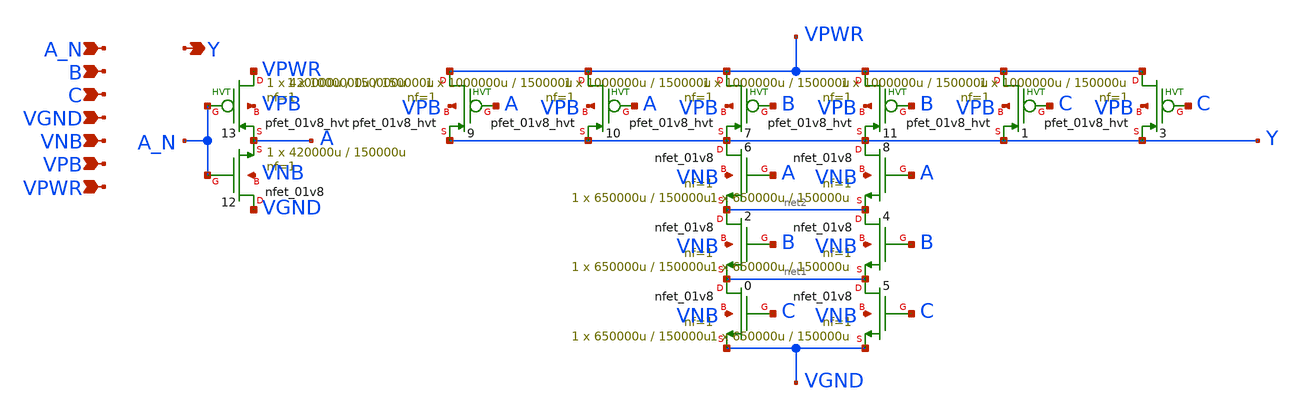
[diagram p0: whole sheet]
** sch_path: schematics/nand3b/sky130_fd_sc_hd__nand3b_2.sch
**.subckt sky130_fd_sc_hd__nand3b_2 A_N B C VGND VNB VPB VPWR Y
*.ipin A_N
*.ipin B
*.ipin C
*.ipin VGND
*.ipin VNB
*.ipin VPB
*.ipin VPWR
*.opin Y
X10 VPWR A Y VPB sky130_fd_pr__pfet_01v8_hvt L=150000u W=1000000u nf=1 ad='int((1 + 1)/2) * 1000000u / 1 * 0.29'
+ as='int((1 + 2)/2) * 1000000u / 1 * 0.29' pd='2*int((1 + 1)/2) * (1000000u / 1 + 0.29)' ps='2*int((1 + 2)/2) * (1000000u / 1 + 0.29)'
+ nrd='0.29 / 1000000u ' nrs='0.29 / 1000000u ' sa=0 sb=0 sd=0 mult=1 m=1
X9 VPWR A Y VPB sky130_fd_pr__pfet_01v8_hvt L=150000u W=1000000u nf=1 ad='int((1 + 1)/2) * 1000000u / 1 * 0.29'
+ as='int((1 + 2)/2) * 1000000u / 1 * 0.29' pd='2*int((1 + 1)/2) * (1000000u / 1 + 0.29)' ps='2*int((1 + 2)/2) * (1000000u / 1 + 0.29)'
+ nrd='0.29 / 1000000u ' nrs='0.29 / 1000000u ' sa=0 sb=0 sd=0 mult=1 m=1
X6 Y A net2 VNB sky130_fd_pr__nfet_01v8 L=150000u W=650000u nf=1 ad='int((1 + 1)/2) * 650000u / 1 * 0.29'
+ as='int((1 + 2)/2) * 650000u / 1 * 0.29' pd='2*int((1 + 1)/2) * (650000u / 1 + 0.29)' ps='2*int((1 + 2)/2) * (650000u / 1 + 0.29)'
+ nrd='0.29 / 650000u ' nrs='0.29 / 650000u ' sa=0 sb=0 sd=0 mult=1 m=1
X2 net2 B net1 VNB sky130_fd_pr__nfet_01v8 L=150000u W=650000u nf=1 ad='int((1 + 1)/2) * 650000u / 1 * 0.29'
+ as='int((1 + 2)/2) * 650000u / 1 * 0.29' pd='2*int((1 + 1)/2) * (650000u / 1 + 0.29)' ps='2*int((1 + 2)/2) * (650000u / 1 + 0.29)'
+ nrd='0.29 / 650000u ' nrs='0.29 / 650000u ' sa=0 sb=0 sd=0 mult=1 m=1
X7 VPWR B Y VPB sky130_fd_pr__pfet_01v8_hvt L=150000u W=1000000u nf=1 ad='int((1 + 1)/2) * 1000000u / 1 * 0.29'
+ as='int((1 + 2)/2) * 1000000u / 1 * 0.29' pd='2*int((1 + 1)/2) * (1000000u / 1 + 0.29)' ps='2*int((1 + 2)/2) * (1000000u / 1 + 0.29)'
+ nrd='0.29 / 1000000u ' nrs='0.29 / 1000000u ' sa=0 sb=0 sd=0 mult=1 m=1
X0 net1 C VGND VNB sky130_fd_pr__nfet_01v8 L=150000u W=650000u nf=1 ad='int((1 + 1)/2) * 650000u / 1 * 0.29'
+ as='int((1 + 2)/2) * 650000u / 1 * 0.29' pd='2*int((1 + 1)/2) * (650000u / 1 + 0.29)' ps='2*int((1 + 2)/2) * (650000u / 1 + 0.29)'
+ nrd='0.29 / 650000u ' nrs='0.29 / 650000u ' sa=0 sb=0 sd=0 mult=1 m=1
X1 VPWR C Y VPB sky130_fd_pr__pfet_01v8_hvt L=150000u W=1000000u nf=1 ad='int((1 + 1)/2) * 1000000u / 1 * 0.29'
+ as='int((1 + 2)/2) * 1000000u / 1 * 0.29' pd='2*int((1 + 1)/2) * (1000000u / 1 + 0.29)' ps='2*int((1 + 2)/2) * (1000000u / 1 + 0.29)'
+ nrd='0.29 / 1000000u ' nrs='0.29 / 1000000u ' sa=0 sb=0 sd=0 mult=1 m=1
X11 VPWR B Y VPB sky130_fd_pr__pfet_01v8_hvt L=150000u W=1000000u nf=1 ad='int((1 + 1)/2) * 1000000u / 1 * 0.29'
+ as='int((1 + 2)/2) * 1000000u / 1 * 0.29' pd='2*int((1 + 1)/2) * (1000000u / 1 + 0.29)' ps='2*int((1 + 2)/2) * (1000000u / 1 + 0.29)'
+ nrd='0.29 / 1000000u ' nrs='0.29 / 1000000u ' sa=0 sb=0 sd=0 mult=1 m=1
X3 VPWR C Y VPB sky130_fd_pr__pfet_01v8_hvt L=150000u W=1000000u nf=1 ad='int((1 + 1)/2) * 1000000u / 1 * 0.29'
+ as='int((1 + 2)/2) * 1000000u / 1 * 0.29' pd='2*int((1 + 1)/2) * (1000000u / 1 + 0.29)' ps='2*int((1 + 2)/2) * (1000000u / 1 + 0.29)'
+ nrd='0.29 / 1000000u ' nrs='0.29 / 1000000u ' sa=0 sb=0 sd=0 mult=1 m=1
X8 Y A net2 VNB sky130_fd_pr__nfet_01v8 L=150000u W=650000u nf=1 ad='int((1 + 1)/2) * 650000u / 1 * 0.29'
+ as='int((1 + 2)/2) * 650000u / 1 * 0.29' pd='2*int((1 + 1)/2) * (650000u / 1 + 0.29)' ps='2*int((1 + 2)/2) * (650000u / 1 + 0.29)'
+ nrd='0.29 / 650000u ' nrs='0.29 / 650000u ' sa=0 sb=0 sd=0 mult=1 m=1
X4 net2 B net1 VNB sky130_fd_pr__nfet_01v8 L=150000u W=650000u nf=1 ad='int((1 + 1)/2) * 650000u / 1 * 0.29'
+ as='int((1 + 2)/2) * 650000u / 1 * 0.29' pd='2*int((1 + 1)/2) * (650000u / 1 + 0.29)' ps='2*int((1 + 2)/2) * (650000u / 1 + 0.29)'
+ nrd='0.29 / 650000u ' nrs='0.29 / 650000u ' sa=0 sb=0 sd=0 mult=1 m=1
X5 net1 C VGND VNB sky130_fd_pr__nfet_01v8 L=150000u W=650000u nf=1 ad='int((1 + 1)/2) * 650000u / 1 * 0.29'
+ as='int((1 + 2)/2) * 650000u / 1 * 0.29' pd='2*int((1 + 1)/2) * (650000u / 1 + 0.29)' ps='2*int((1 + 2)/2) * (650000u / 1 + 0.29)'
+ nrd='0.29 / 650000u ' nrs='0.29 / 650000u ' sa=0 sb=0 sd=0 mult=1 m=1
X12 VGND A_N A VNB sky130_fd_pr__nfet_01v8 L=150000u W=420000u nf=1 ad='int((1 + 1)/2) * 420000u / 1 * 0.29'
+ as='int((1 + 2)/2) * 420000u / 1 * 0.29' pd='2*int((1 + 1)/2) * (420000u / 1 + 0.29)' ps='2*int((1 + 2)/2) * (420000u / 1 + 0.29)'
+ nrd='0.29 / 420000u ' nrs='0.29 / 420000u ' sa=0 sb=0 sd=0 mult=1 m=1
X13 VPWR A_N A VPB sky130_fd_pr__pfet_01v8_hvt L=150000u W=420000u nf=1 ad='int((1 + 1)/2) * 420000u / 1 * 0.29'
+ as='int((1 + 2)/2) * 420000u / 1 * 0.29' pd='2*int((1 + 1)/2) * (420000u / 1 + 0.29)' ps='2*int((1 + 2)/2) * (420000u / 1 + 0.29)'
+ nrd='0.29 / 420000u ' nrs='0.29 / 420000u ' sa=0 sb=0 sd=0 mult=1 m=1
**.ends
.end
